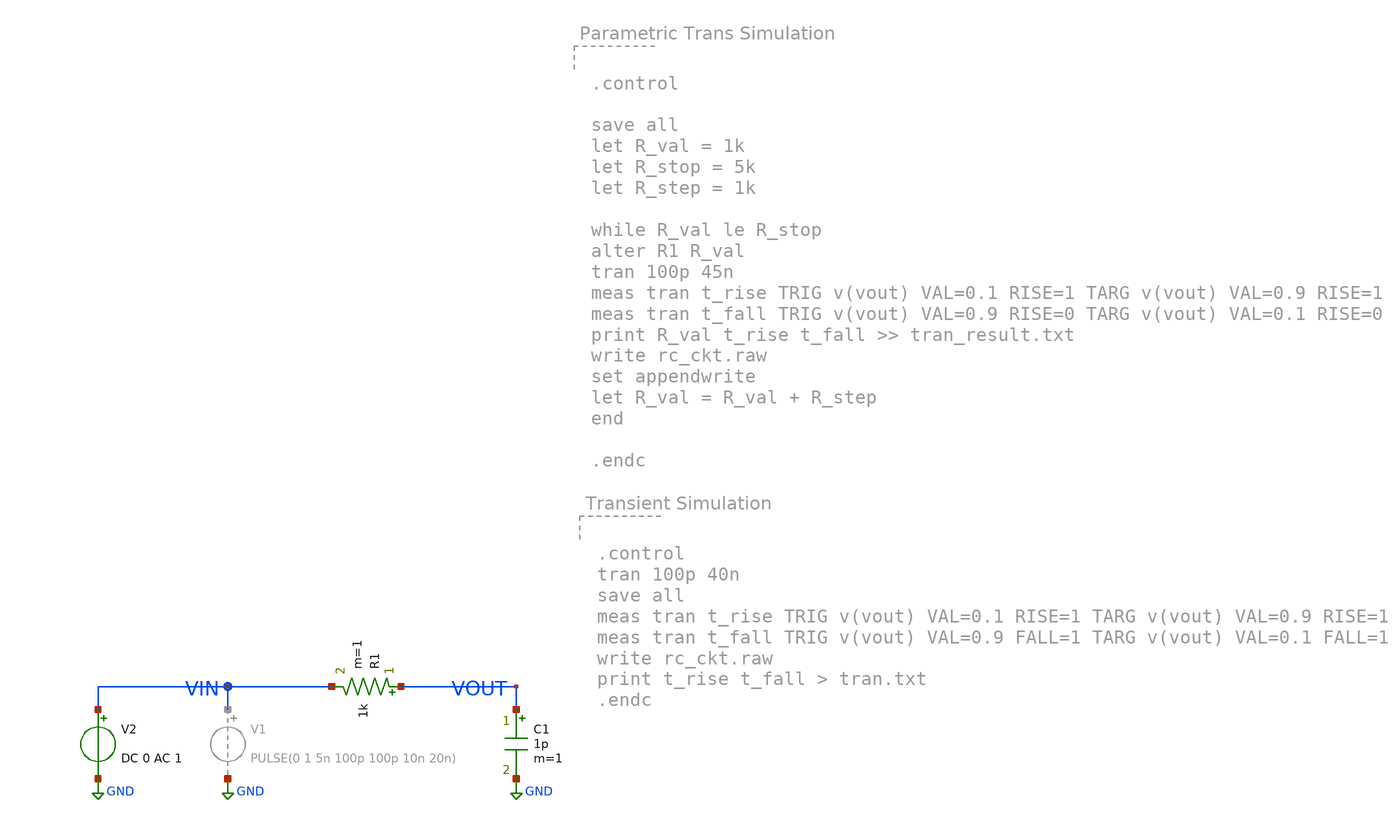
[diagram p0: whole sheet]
** sch_path: ITI_Labs/Lab1/RC/Design/RC.sch
**.subckt RC
C1 VOUT GND 1p m=1
R1 VOUT VIN 1k m=1
V2 VIN GND DC 0 AC 1
**** begin user architecture code


.control
ac dec 10 1 10G
save all
meas ac MAX_GAIN MAX vmag(vout) from=1 to=10G
meas ac BW when vmag(vout)=0.707 fall = 1
write rc_ckt_ac.raw
set appendwrite
touch ac_results.txt
print MAX_GAIN BW > ac_results.txt
.endc


**** end user architecture code
**.ends
.GLOBAL GND
.end
